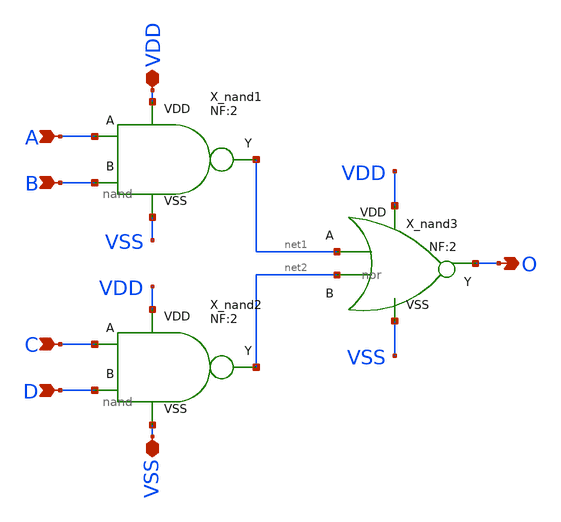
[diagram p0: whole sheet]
** sch_path: xschem_lib/sylee21/and_4in.sch
**.subckt and_4in VDD VSS A B C D O
*.iopin VDD
*.iopin VSS
*.ipin A
*.ipin B
*.ipin C
*.ipin D
*.opin O
X_nand2 D C net2 VDD VSS nand NF=2
X_nand1 B A net1 VDD VSS nand NF=2
X_nand3 O net1 net2 VDD VSS nor NF=2
**.ends

* expanding   symbol:
*+  /Users/brianlsy/Desktop/brianlsy/git_workspace/fork/laygo2_workspace_sky130/xschem_lib/sylee21/nand.sym # of pins=5
** sym_path: xschem_lib/sylee21/nand.sym
** sch_path: xschem_lib/sylee21/nand.sch
.subckt nand B A Y VDD VSS  NF=2
*.opin Y
*.ipin A
*.iopin VDD
*.iopin VSS
*.ipin B
XM1 Y A net1 VSS sky130_fd_pr__nfet_01v8_lvt L=0.15 W=1.2 nf=1 ad='int((nf+1)/2) * W/nf * 0.29' as='int((nf+2)/2) * W/nf * 0.29'
+ pd='2*int((nf+1)/2) * (W/nf + 0.29)' ps='2*int((nf+2)/2) * (W/nf + 0.29)' nrd='0.29 / W' nrs='0.29 / W'
+ sa=0 sb=0 sd=0 mult=NF m=NF
XM2 net1 B VSS VSS sky130_fd_pr__nfet_01v8_lvt L=0.15 W=1.2 nf=1 ad='int((nf+1)/2) * W/nf * 0.29' as='int((nf+2)/2) * W/nf * 0.29'
+ pd='2*int((nf+1)/2) * (W/nf + 0.29)' ps='2*int((nf+2)/2) * (W/nf + 0.29)' nrd='0.29 / W' nrs='0.29 / W'
+ sa=0 sb=0 sd=0 mult=NF m=NF
XM3 Y B VDD VDD sky130_fd_pr__pfet_01v8 L=0.15 W=2.4 nf=1 ad='int((nf+1)/2) * W/nf * 0.29' as='int((nf+2)/2) * W/nf * 0.29'
+ pd='2*int((nf+1)/2) * (W/nf + 0.29)' ps='2*int((nf+2)/2) * (W/nf + 0.29)' nrd='0.29 / W' nrs='0.29 / W'
+ sa=0 sb=0 sd=0 mult=NF m=NF
XM4 Y A VDD VDD sky130_fd_pr__pfet_01v8 L=0.15 W=2.4 nf=1 ad='int((nf+1)/2) * W/nf * 0.29' as='int((nf+2)/2) * W/nf * 0.29'
+ pd='2*int((nf+1)/2) * (W/nf + 0.29)' ps='2*int((nf+2)/2) * (W/nf + 0.29)' nrd='0.29 / W' nrs='0.29 / W'
+ sa=0 sb=0 sd=0 mult=NF m=NF
.ends


* expanding   symbol:
*+  /Users/brianlsy/Desktop/brianlsy/git_workspace/fork/laygo2_workspace_sky130/xschem_lib/sylee21/nor.sym # of pins=5
** sym_path: xschem_lib/DFFRAM_full_custom/nor.sym
** sch_path: xschem_lib/DFFRAM_full_custom/nor.sch
.subckt nor Y A B VDD VSS  NF=2
*.iopin VDD
*.iopin VSS
*.opin Y
*.ipin A
*.ipin B
XM1 Y B VSS VSS sky130_fd_pr__nfet_01v8_lvt L=0.15 W=NF*1.2 nf=NF ad='int((nf+1)/2) * W/nf * 0.29' as='int((nf+2)/2) * W/nf * 0.29'
+ pd='2*int((nf+1)/2) * (W/nf + 0.29)' ps='2*int((nf+2)/2) * (W/nf + 0.29)' nrd='0.29 / W' nrs='0.29 / W'
+ sa=0 sb=0 sd=0 mult=1 m=1
XM4 net1 B VDD VDD sky130_fd_pr__pfet_01v8 L=0.15 W=NF*2.4 nf=NF ad='int((nf+1)/2) * W/nf * 0.29' as='int((nf+2)/2) * W/nf * 0.29'
+ pd='2*int((nf+1)/2) * (W/nf + 0.29)' ps='2*int((nf+2)/2) * (W/nf + 0.29)' nrd='0.29 / W' nrs='0.29 / W'
+ sa=0 sb=0 sd=0 mult=1 m=1
XM3 Y A net1 VDD sky130_fd_pr__pfet_01v8 L=0.15 W=NF*2.4 nf=NF ad='int((nf+1)/2) * W/nf * 0.29' as='int((nf+2)/2) * W/nf * 0.29'
+ pd='2*int((nf+1)/2) * (W/nf + 0.29)' ps='2*int((nf+2)/2) * (W/nf + 0.29)' nrd='0.29 / W' nrs='0.29 / W'
+ sa=0 sb=0 sd=0 mult=1 m=1
XM2 Y A VSS VSS sky130_fd_pr__nfet_01v8_lvt L=0.15 W=NF*1.2 nf=NF ad='int((nf+1)/2) * W/nf * 0.29' as='int((nf+2)/2) * W/nf * 0.29'
+ pd='2*int((nf+1)/2) * (W/nf + 0.29)' ps='2*int((nf+2)/2) * (W/nf + 0.29)' nrd='0.29 / W' nrs='0.29 / W'
+ sa=0 sb=0 sd=0 mult=1 m=1
.ends

.end
